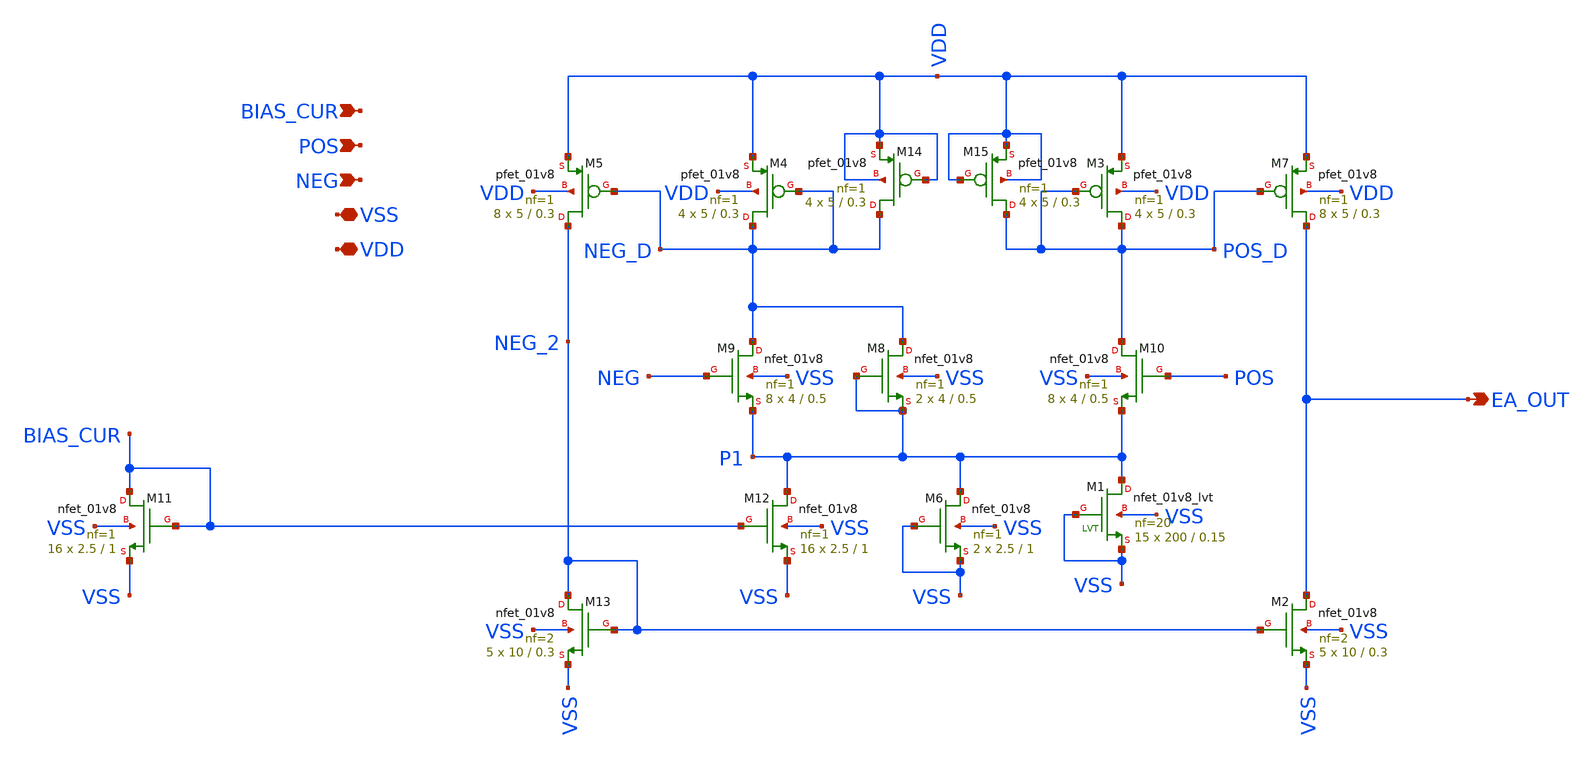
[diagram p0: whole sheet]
** sch_path: xschem/opamp.sch
**.subckt opamp POS NEG VDD VSS BIAS_CUR EA_OUT
*.ipin POS
*.ipin NEG
*.iopin VDD
*.iopin VSS
*.ipin BIAS_CUR
*.opin EA_OUT
XM3 POS_D POS_D VDD VDD sky130_fd_pr__pfet_01v8 L=0.3 W=5 nf=1 ad='int((nf+1)/2) * W/nf * 0.29' as='int((nf+2)/2) * W/nf * 0.29'
+ pd='2*int((nf+1)/2) * (W/nf + 0.29)' ps='2*int((nf+2)/2) * (W/nf + 0.29)' nrd='0.29 / W' nrs='0.29 / W'
+ sa=0 sb=0 sd=0 mult=4 m=4
XM4 NEG_D NEG_D VDD VDD sky130_fd_pr__pfet_01v8 L=0.3 W=5 nf=1 ad='int((nf+1)/2) * W/nf * 0.29' as='int((nf+2)/2) * W/nf * 0.29'
+ pd='2*int((nf+1)/2) * (W/nf + 0.29)' ps='2*int((nf+2)/2) * (W/nf + 0.29)' nrd='0.29 / W' nrs='0.29 / W'
+ sa=0 sb=0 sd=0 mult=4 m=4
XM5 NEG_2 NEG_D VDD VDD sky130_fd_pr__pfet_01v8 L=0.3 W=5 nf=1 ad='int((nf+1)/2) * W/nf * 0.29' as='int((nf+2)/2) * W/nf * 0.29'
+ pd='2*int((nf+1)/2) * (W/nf + 0.29)' ps='2*int((nf+2)/2) * (W/nf + 0.29)' nrd='0.29 / W' nrs='0.29 / W'
+ sa=0 sb=0 sd=0 mult=8 m=8
XM7 EA_OUT POS_D VDD VDD sky130_fd_pr__pfet_01v8 L=0.3 W=5 nf=1 ad='int((nf+1)/2) * W/nf * 0.29' as='int((nf+2)/2) * W/nf * 0.29'
+ pd='2*int((nf+1)/2) * (W/nf + 0.29)' ps='2*int((nf+2)/2) * (W/nf + 0.29)' nrd='0.29 / W' nrs='0.29 / W'
+ sa=0 sb=0 sd=0 mult=8 m=8
XM9 NEG_D NEG P1 VSS sky130_fd_pr__nfet_01v8 L=0.5 W=4 nf=1 ad='int((nf+1)/2) * W/nf * 0.29' as='int((nf+2)/2) * W/nf * 0.29'
+ pd='2*int((nf+1)/2) * (W/nf + 0.29)' ps='2*int((nf+2)/2) * (W/nf + 0.29)' nrd='0.29 / W' nrs='0.29 / W'
+ sa=0 sb=0 sd=0 mult=8 m=8
XM10 POS_D POS P1 VSS sky130_fd_pr__nfet_01v8 L=0.5 W=4 nf=1 ad='int((nf+1)/2) * W/nf * 0.29' as='int((nf+2)/2) * W/nf * 0.29'
+ pd='2*int((nf+1)/2) * (W/nf + 0.29)' ps='2*int((nf+2)/2) * (W/nf + 0.29)' nrd='0.29 / W' nrs='0.29 / W'
+ sa=0 sb=0 sd=0 mult=8 m=8
XM11 BIAS_CUR BIAS_CUR VSS VSS sky130_fd_pr__nfet_01v8 L=1 W=2.5 nf=1 ad='int((nf+1)/2) * W/nf * 0.29'
+ as='int((nf+2)/2) * W/nf * 0.29' pd='2*int((nf+1)/2) * (W/nf + 0.29)' ps='2*int((nf+2)/2) * (W/nf + 0.29)'
+ nrd='0.29 / W' nrs='0.29 / W' sa=0 sb=0 sd=0 mult=16 m=16
XM12 P1 BIAS_CUR VSS VSS sky130_fd_pr__nfet_01v8 L=1 W=2.5 nf=1 ad='int((nf+1)/2) * W/nf * 0.29' as='int((nf+2)/2) * W/nf * 0.29'
+ pd='2*int((nf+1)/2) * (W/nf + 0.29)' ps='2*int((nf+2)/2) * (W/nf + 0.29)' nrd='0.29 / W' nrs='0.29 / W'
+ sa=0 sb=0 sd=0 mult=16 m=16
XM13 NEG_2 NEG_2 VSS VSS sky130_fd_pr__nfet_01v8 L=0.3 W=10 nf=2 ad='int((nf+1)/2) * W/nf * 0.29' as='int((nf+2)/2) * W/nf * 0.29'
+ pd='2*int((nf+1)/2) * (W/nf + 0.29)' ps='2*int((nf+2)/2) * (W/nf + 0.29)' nrd='0.29 / W' nrs='0.29 / W'
+ sa=0 sb=0 sd=0 mult=5 m=5
XM1 P1 VSS VSS VSS sky130_fd_pr__nfet_01v8_lvt L=0.15 W=200 nf=20 ad='int((nf+1)/2) * W/nf * 0.29' as='int((nf+2)/2) * W/nf * 0.29'
+ pd='2*int((nf+1)/2) * (W/nf + 0.29)' ps='2*int((nf+2)/2) * (W/nf + 0.29)' nrd='0.29 / W' nrs='0.29 / W'
+ sa=0 sb=0 sd=0 mult=15 m=15
XM2 EA_OUT NEG_2 VSS VSS sky130_fd_pr__nfet_01v8 L=0.3 W=10 nf=2 ad='int((nf+1)/2) * W/nf * 0.29' as='int((nf+2)/2) * W/nf * 0.29'
+ pd='2*int((nf+1)/2) * (W/nf + 0.29)' ps='2*int((nf+2)/2) * (W/nf + 0.29)' nrd='0.29 / W' nrs='0.29 / W'
+ sa=0 sb=0 sd=0 mult=5 m=5
XM6 P1 VSS VSS VSS sky130_fd_pr__nfet_01v8 L=1 W=2.5 nf=1 ad='int((nf+1)/2) * W/nf * 0.29' as='int((nf+2)/2) * W/nf * 0.29'
+ pd='2*int((nf+1)/2) * (W/nf + 0.29)' ps='2*int((nf+2)/2) * (W/nf + 0.29)' nrd='0.29 / W' nrs='0.29 / W'
+ sa=0 sb=0 sd=0 mult=2 m=2
XM8 NEG_D P1 P1 VSS sky130_fd_pr__nfet_01v8 L=0.5 W=4 nf=1 ad='int((nf+1)/2) * W/nf * 0.29' as='int((nf+2)/2) * W/nf * 0.29'
+ pd='2*int((nf+1)/2) * (W/nf + 0.29)' ps='2*int((nf+2)/2) * (W/nf + 0.29)' nrd='0.29 / W' nrs='0.29 / W'
+ sa=0 sb=0 sd=0 mult=2 m=2
XM14 NEG_D VDD VDD VDD sky130_fd_pr__pfet_01v8 L=0.3 W=5 nf=1 ad='int((nf+1)/2) * W/nf * 0.29' as='int((nf+2)/2) * W/nf * 0.29'
+ pd='2*int((nf+1)/2) * (W/nf + 0.29)' ps='2*int((nf+2)/2) * (W/nf + 0.29)' nrd='0.29 / W' nrs='0.29 / W'
+ sa=0 sb=0 sd=0 mult=4 m=4
XM15 POS_D VDD VDD VDD sky130_fd_pr__pfet_01v8 L=0.3 W=5 nf=1 ad='int((nf+1)/2) * W/nf * 0.29' as='int((nf+2)/2) * W/nf * 0.29'
+ pd='2*int((nf+1)/2) * (W/nf + 0.29)' ps='2*int((nf+2)/2) * (W/nf + 0.29)' nrd='0.29 / W' nrs='0.29 / W'
+ sa=0 sb=0 sd=0 mult=4 m=4
**.ends
.end
